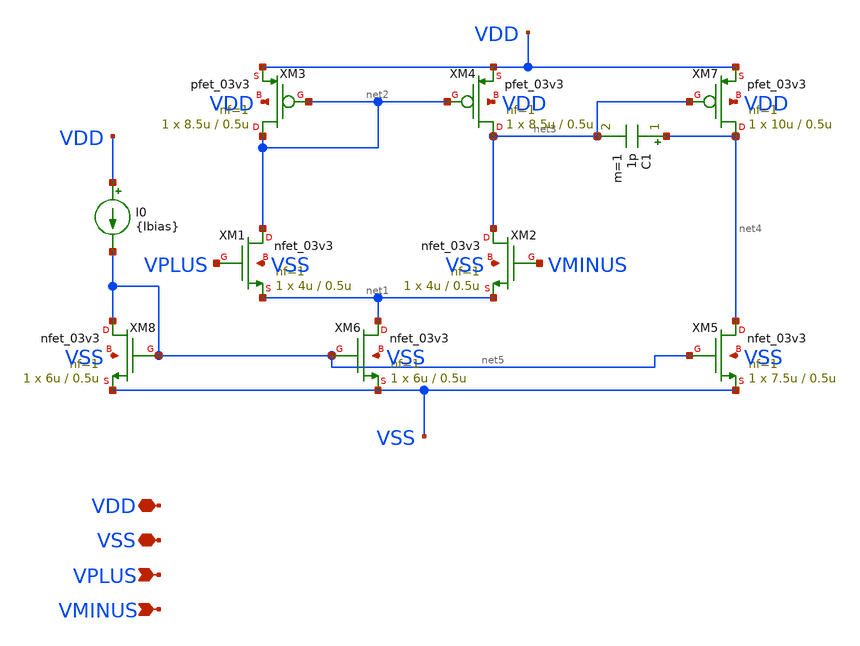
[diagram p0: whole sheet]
** sch_path: xschem/buffer.sch
**.subckt buffer VDD VSS VPLUS VMINUS
*.iopin VDD
*.iopin VSS
*.ipin VPLUS
*.ipin VMINUS
XM1 net2 VPLUS net1 VSS nfet_03v3 L=0.5u W=4u nf=1 ad='int((nf+1)/2) * W/nf * 0.18u' as='int((nf+2)/2) * W/nf * 0.18u'
+ pd='2*int((nf+1)/2) * (W/nf + 0.18u)' ps='2*int((nf+2)/2) * (W/nf + 0.18u)' nrd='0.18u / W' nrs='0.18u / W'
+ sa=0 sb=0 sd=0 m=1
XM2 net3 VMINUS net1 VSS nfet_03v3 L=0.5u W=4u nf=1 ad='int((nf+1)/2) * W/nf * 0.18u' as='int((nf+2)/2) * W/nf * 0.18u'
+ pd='2*int((nf+1)/2) * (W/nf + 0.18u)' ps='2*int((nf+2)/2) * (W/nf + 0.18u)' nrd='0.18u / W' nrs='0.18u / W'
+ sa=0 sb=0 sd=0 m=1
XM3 net2 net2 VDD VDD pfet_03v3 L=0.5u W=8.5u nf=1 ad='int((nf+1)/2) * W/nf * 0.18u' as='int((nf+2)/2) * W/nf * 0.18u'
+ pd='2*int((nf+1)/2) * (W/nf + 0.18u)' ps='2*int((nf+2)/2) * (W/nf + 0.18u)' nrd='0.18u / W' nrs='0.18u / W'
+ sa=0 sb=0 sd=0 m=1
XM4 net3 net2 VDD VDD pfet_03v3 L=0.5u W=8.5u nf=1 ad='int((nf+1)/2) * W/nf * 0.18u' as='int((nf+2)/2) * W/nf * 0.18u'
+ pd='2*int((nf+1)/2) * (W/nf + 0.18u)' ps='2*int((nf+2)/2) * (W/nf + 0.18u)' nrd='0.18u / W' nrs='0.18u / W'
+ sa=0 sb=0 sd=0 m=1
XM5 net4 net5 VSS VSS nfet_03v3 L=0.5u W=7.5u nf=1 ad='int((nf+1)/2) * W/nf * 0.18u' as='int((nf+2)/2) * W/nf * 0.18u'
+ pd='2*int((nf+1)/2) * (W/nf + 0.18u)' ps='2*int((nf+2)/2) * (W/nf + 0.18u)' nrd='0.18u / W' nrs='0.18u / W'
+ sa=0 sb=0 sd=0 m=1
C1 net4 net3 1p m=1
XM6 net1 net5 VSS VSS nfet_03v3 L=0.5u W=6u nf=1 ad='int((nf+1)/2) * W/nf * 0.18u' as='int((nf+2)/2) * W/nf * 0.18u'
+ pd='2*int((nf+1)/2) * (W/nf + 0.18u)' ps='2*int((nf+2)/2) * (W/nf + 0.18u)' nrd='0.18u / W' nrs='0.18u / W'
+ sa=0 sb=0 sd=0 m=1
XM7 net4 net3 VDD VDD pfet_03v3 L=0.5u W=10u nf=1 ad='int((nf+1)/2) * W/nf * 0.18u' as='int((nf+2)/2) * W/nf * 0.18u'
+ pd='2*int((nf+1)/2) * (W/nf + 0.18u)' ps='2*int((nf+2)/2) * (W/nf + 0.18u)' nrd='0.18u / W' nrs='0.18u / W'
+ sa=0 sb=0 sd=0 m=1
XM8 net5 net5 VSS VSS nfet_03v3 L=0.5u W=6u nf=1 ad='int((nf+1)/2) * W/nf * 0.18u' as='int((nf+2)/2) * W/nf * 0.18u'
+ pd='2*int((nf+1)/2) * (W/nf + 0.18u)' ps='2*int((nf+2)/2) * (W/nf + 0.18u)' nrd='0.18u / W' nrs='0.18u / W'
+ sa=0 sb=0 sd=0 m=1
I0 VDD net5 {Ibias}
**.ends
.end
